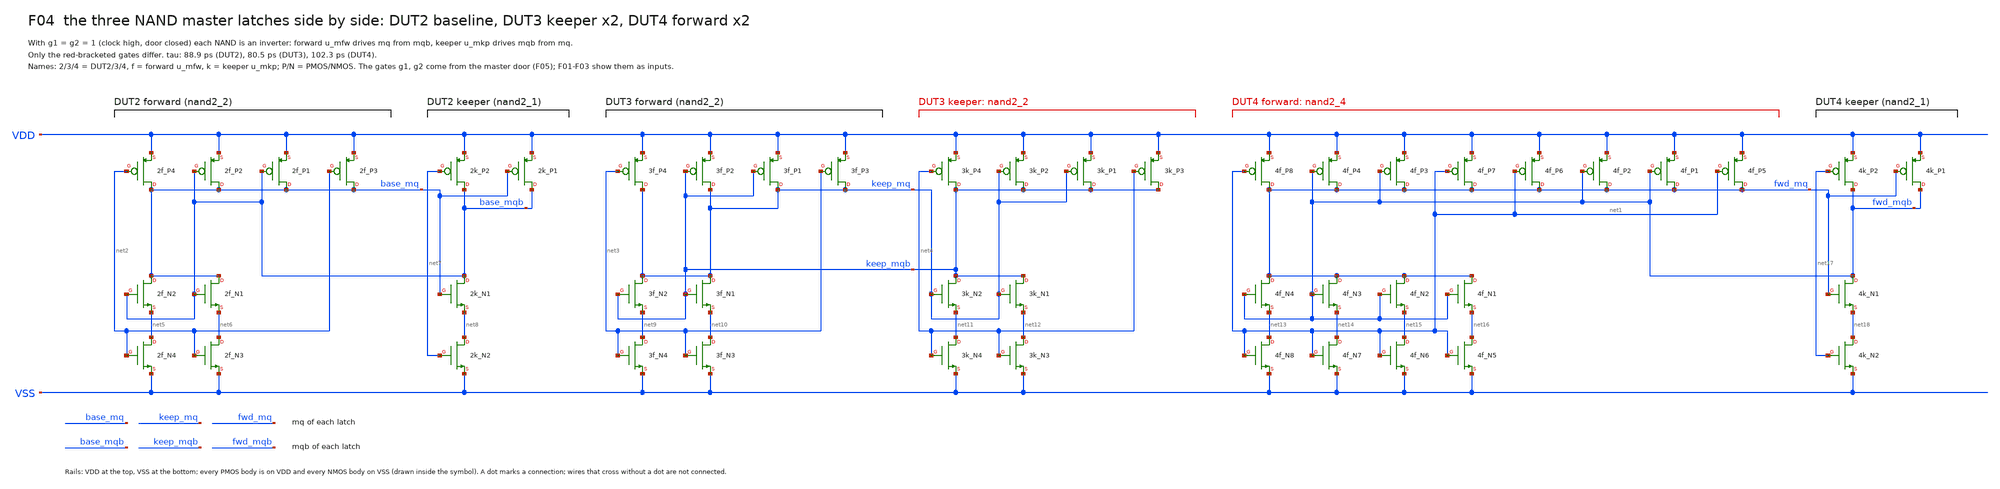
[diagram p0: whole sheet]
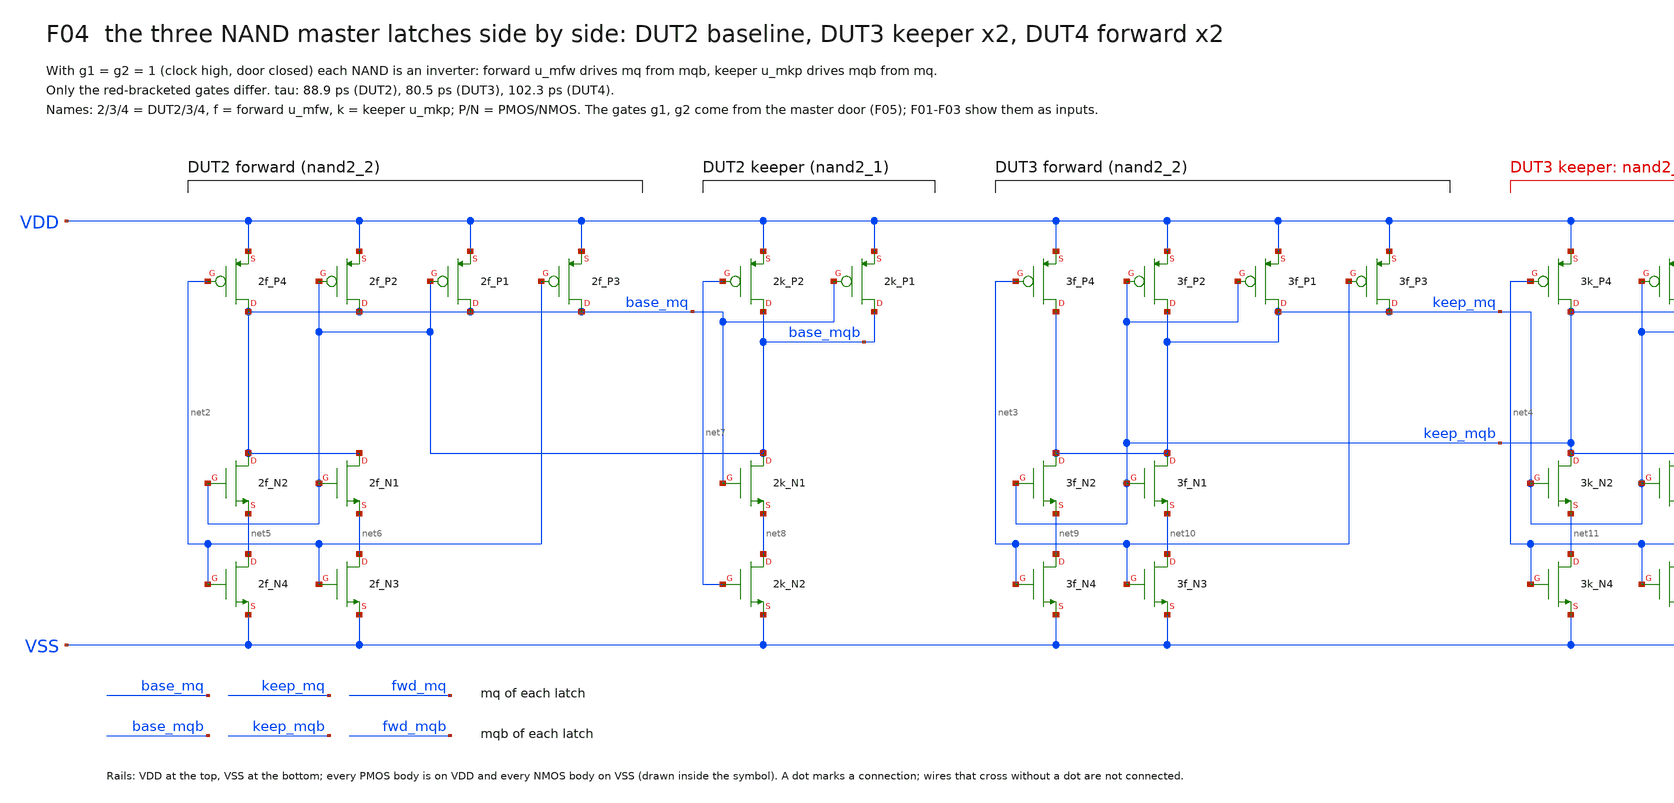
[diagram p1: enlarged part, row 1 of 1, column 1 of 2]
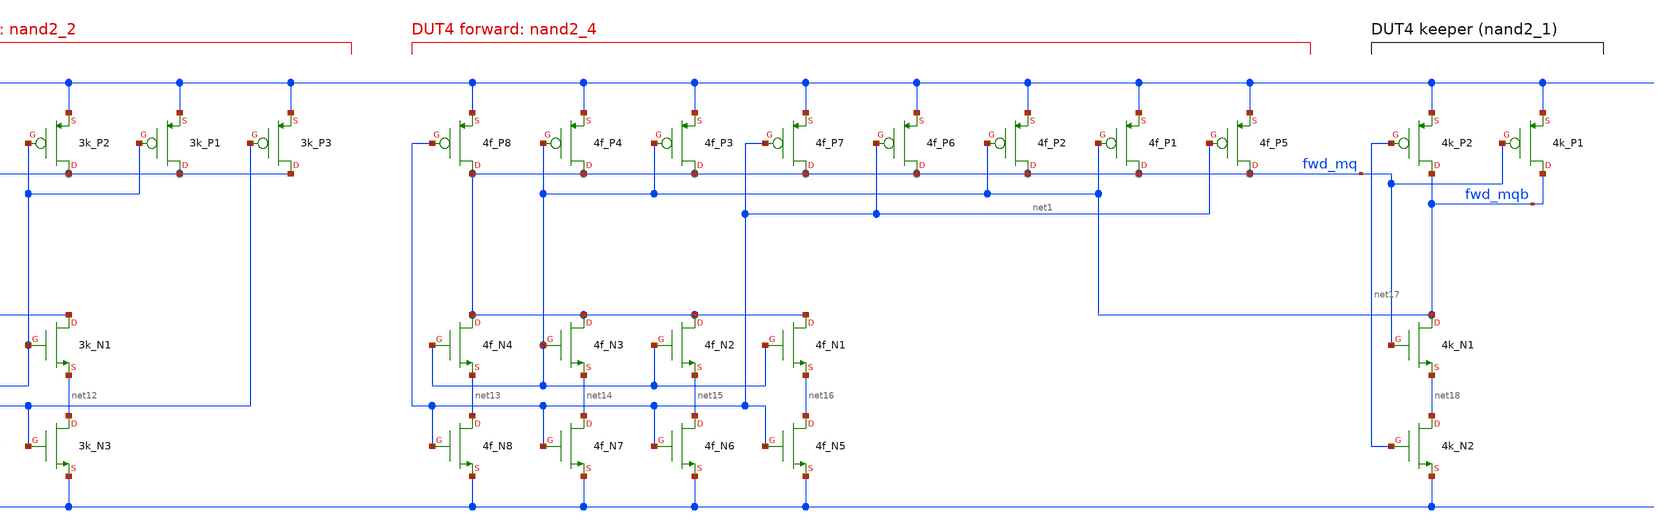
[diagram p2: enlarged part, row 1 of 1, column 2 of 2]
** sch_path: xschem/focus/F04_master_latch_comparison.sch
**.subckt F04_master_latch_comparison
X2f_N4 net5 net2 VSS VSS nfet_05v0 L=0.6u W=0.82u nf=1 m=1
X2f_N2 base_mq base_mqb net5 VSS nfet_05v0 L=0.6u W=0.82u nf=1 m=1
X2f_N1 base_mq base_mqb net6 VSS nfet_05v0 L=0.6u W=0.82u nf=1 m=1
X2f_N3 net6 net2 VSS VSS nfet_05v0 L=0.6u W=0.82u nf=1 m=1
X2f_P4 base_mq net2 VDD VDD pfet_05v0 L=0.5u W=1.13u nf=1 m=1
X2f_P2 base_mq base_mqb VDD VDD pfet_05v0 L=0.5u W=1.13u nf=1 m=1
X2f_P1 base_mq base_mqb VDD VDD pfet_05v0 L=0.5u W=1.13u nf=1 m=1
X2f_P3 base_mq net2 VDD VDD pfet_05v0 L=0.5u W=1.13u nf=1 m=1
X2k_N2 net8 net7 VSS VSS nfet_05v0 L=0.6u W=0.82u nf=1 m=1
X2k_N1 base_mqb base_mq net8 VSS nfet_05v0 L=0.6u W=0.82u nf=1 m=1
X2k_P2 base_mqb net7 VDD VDD pfet_05v0 L=0.5u W=1.13u nf=1 m=1
X2k_P1 base_mqb base_mq VDD VDD pfet_05v0 L=0.5u W=1.13u nf=1 m=1
X3f_N4 net9 net3 VSS VSS nfet_05v0 L=0.6u W=0.82u nf=1 m=1
X3f_N2 keep_mq keep_mqb net9 VSS nfet_05v0 L=0.6u W=0.82u nf=1 m=1
X3f_N1 keep_mq keep_mqb net10 VSS nfet_05v0 L=0.6u W=0.82u nf=1 m=1
X3f_N3 net10 net3 VSS VSS nfet_05v0 L=0.6u W=0.82u nf=1 m=1
X3f_P4 keep_mq net3 VDD VDD pfet_05v0 L=0.5u W=1.13u nf=1 m=1
X3f_P2 keep_mq keep_mqb VDD VDD pfet_05v0 L=0.5u W=1.13u nf=1 m=1
X3f_P1 keep_mq keep_mqb VDD VDD pfet_05v0 L=0.5u W=1.13u nf=1 m=1
X3f_P3 keep_mq net3 VDD VDD pfet_05v0 L=0.5u W=1.13u nf=1 m=1
X3k_N4 net11 net4 VSS VSS nfet_05v0 L=0.6u W=0.82u nf=1 m=1
X3k_N2 keep_mqb keep_mq net11 VSS nfet_05v0 L=0.6u W=0.82u nf=1 m=1
X3k_N1 keep_mqb keep_mq net12 VSS nfet_05v0 L=0.6u W=0.82u nf=1 m=1
X3k_N3 net12 net4 VSS VSS nfet_05v0 L=0.6u W=0.82u nf=1 m=1
X3k_P4 keep_mqb net4 VDD VDD pfet_05v0 L=0.5u W=1.13u nf=1 m=1
X3k_P2 keep_mqb keep_mq VDD VDD pfet_05v0 L=0.5u W=1.13u nf=1 m=1
X3k_P1 keep_mqb keep_mq VDD VDD pfet_05v0 L=0.5u W=1.13u nf=1 m=1
X3k_P3 keep_mqb net4 VDD VDD pfet_05v0 L=0.5u W=1.13u nf=1 m=1
X4f_N8 net13 net1 VSS VSS nfet_05v0 L=0.6u W=0.82u nf=1 m=1
X4f_N4 fwd_mq fwd_mqb net13 VSS nfet_05v0 L=0.6u W=0.82u nf=1 m=1
X4f_N3 fwd_mq fwd_mqb net14 VSS nfet_05v0 L=0.6u W=0.82u nf=1 m=1
X4f_N7 net14 net1 VSS VSS nfet_05v0 L=0.6u W=0.82u nf=1 m=1
X4f_N6 net15 net1 VSS VSS nfet_05v0 L=0.6u W=0.82u nf=1 m=1
X4f_N2 fwd_mq fwd_mqb net15 VSS nfet_05v0 L=0.6u W=0.82u nf=1 m=1
X4f_N1 fwd_mq fwd_mqb net16 VSS nfet_05v0 L=0.6u W=0.82u nf=1 m=1
X4f_N5 net16 net1 VSS VSS nfet_05v0 L=0.6u W=0.82u nf=1 m=1
X4f_P8 fwd_mq net1 VDD VDD pfet_05v0 L=0.5u W=1.13u nf=1 m=1
X4f_P4 fwd_mq fwd_mqb VDD VDD pfet_05v0 L=0.5u W=1.13u nf=1 m=1
X4f_P3 fwd_mq fwd_mqb VDD VDD pfet_05v0 L=0.5u W=1.13u nf=1 m=1
X4f_P7 fwd_mq net1 VDD VDD pfet_05v0 L=0.5u W=1.13u nf=1 m=1
X4f_P6 fwd_mq net1 VDD VDD pfet_05v0 L=0.5u W=1.13u nf=1 m=1
X4f_P2 fwd_mq fwd_mqb VDD VDD pfet_05v0 L=0.5u W=1.13u nf=1 m=1
X4f_P1 fwd_mq fwd_mqb VDD VDD pfet_05v0 L=0.5u W=1.13u nf=1 m=1
X4f_P5 fwd_mq net1 VDD VDD pfet_05v0 L=0.5u W=1.13u nf=1 m=1
X4k_N2 net18 net17 VSS VSS nfet_05v0 L=0.6u W=0.82u nf=1 m=1
X4k_N1 fwd_mqb fwd_mq net18 VSS nfet_05v0 L=0.6u W=0.82u nf=1 m=1
X4k_P2 fwd_mqb net17 VDD VDD pfet_05v0 L=0.5u W=1.13u nf=1 m=1
X4k_P1 fwd_mqb fwd_mq VDD VDD pfet_05v0 L=0.5u W=1.13u nf=1 m=1
**.ends
.end
